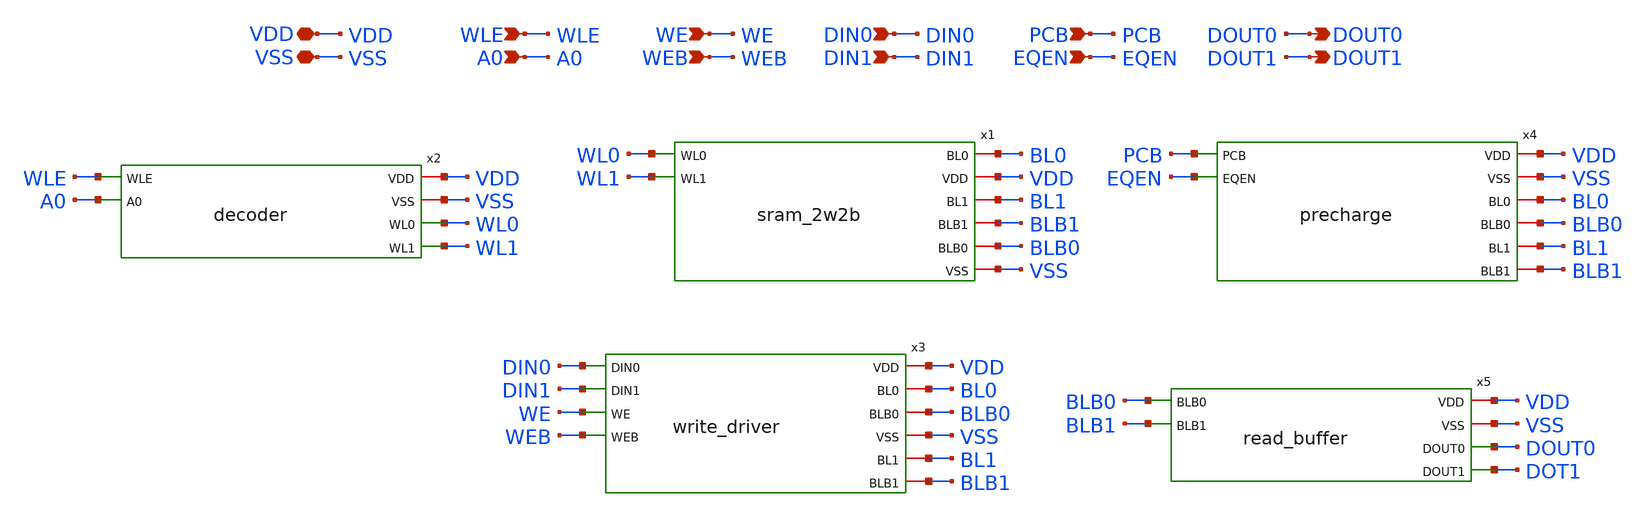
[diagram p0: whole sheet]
** sch_path: array/2word_x_2bit/sram_2w2b_top.sch
**.subckt sram_2w2b_top VDD WLE DOUT0 VSS A0 WE WEB DIN0 DIN1 PCB EQEN DOUT1
*.iopin VDD
*.ipin WLE
*.opin DOUT0
*.iopin VSS
*.ipin A0
*.ipin WE
*.ipin WEB
*.ipin DIN0
*.ipin DIN1
*.ipin PCB
*.ipin EQEN
*.opin DOUT1
x1 WL0 BL0 VDD BL1 BLB1 WL1 BLB0 VSS sram_2w2b
x2 VDD VSS WL0 WLE A0 WL1 decoder
x3 DIN0 VDD BL0 BLB0 VSS DIN1 BL1 WE BLB1 WEB write_driver
x4 VDD VSS PCB EQEN BL0 BLB0 BL1 BLB1 precharge
x5 VDD VSS BLB0 BLB1 DOUT0 DOT1 read_buffer
**.ends
.end
